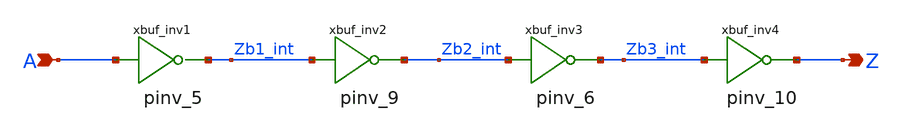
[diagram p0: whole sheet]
** sch_path: sram_4_16_scn4m/pdriver_1.sch
**.subckt pdriver_1 A Z
*.ipin A
*.opin Z
xbuf_inv1 A Zb1_int vdd gnd pinv_5
xbuf_inv2 Zb1_int Zb2_int vdd gnd pinv_9
xbuf_inv3 Zb2_int Zb3_int vdd gnd pinv_6
xbuf_inv4 Zb3_int Z vdd gnd pinv_10
**.ends

* expanding   symbol:  pinv_5.sym # of pins=2
** sym_path: sram_2_16_scn4m/pinv_5.sym
** sch_path: sram_2_16_scn4m/pinv_5.sch
.subckt pinv_5 A Z vdd gnd
*.ipin A
*.opin Z
Mpinv_nmos Z A gnd gnd n w=0.8u l=0.4u m=1
Mp_inv_pmos Z A vdd vdd p w=1.6u l=0.4u m=1
.ends


* expanding   symbol:  pinv_9.sym # of pins=2
** sym_path: sram_2_16_scn4m/pinv_9.sym
** sch_path: sram_2_16_scn4m/pinv_9.sch
.subckt pinv_9 A Z vdd gnd
*.ipin A
*.opin Z
Mpinv_nmos Z A gnd gnd n w=4.0u l=0.4u m=2
Mp_inv_pmos Z A vdd vdd p w=8.0u l=0.4u m=2
.ends


* expanding   symbol:  pinv_6.sym # of pins=2
** sym_path: sram_2_64_scn4m/pinv_6.sym
** sch_path: sram_2_64_scn4m/pinv_6.sch
.subckt pinv_6 A Z vdd gnd
*.ipin A
*.opin Z
Mpinv_nmos Z A gnd gnd n w=3.2u l=0.4u m=1
Mp_inv_pmos Z A vdd vdd p w=6.4u l=0.4u m=1
.ends


* expanding   symbol:  pinv_10.sym # of pins=2
** sym_path: sram_2_16_scn4m/pinv_10.sym
** sch_path: sram_2_16_scn4m/pinv_10.sch
.subckt pinv_10 A Z vdd gnd
*.ipin A
*.opin Z
*.iopin vdd
*.iopin gnd
Mpinv_nmos Z A gnd gnd n w=1.6u l=0.4u m=1
Mpinv_pmos Z A vdd vdd p w=3.2u l=0.4u m=1
.ends

.end
